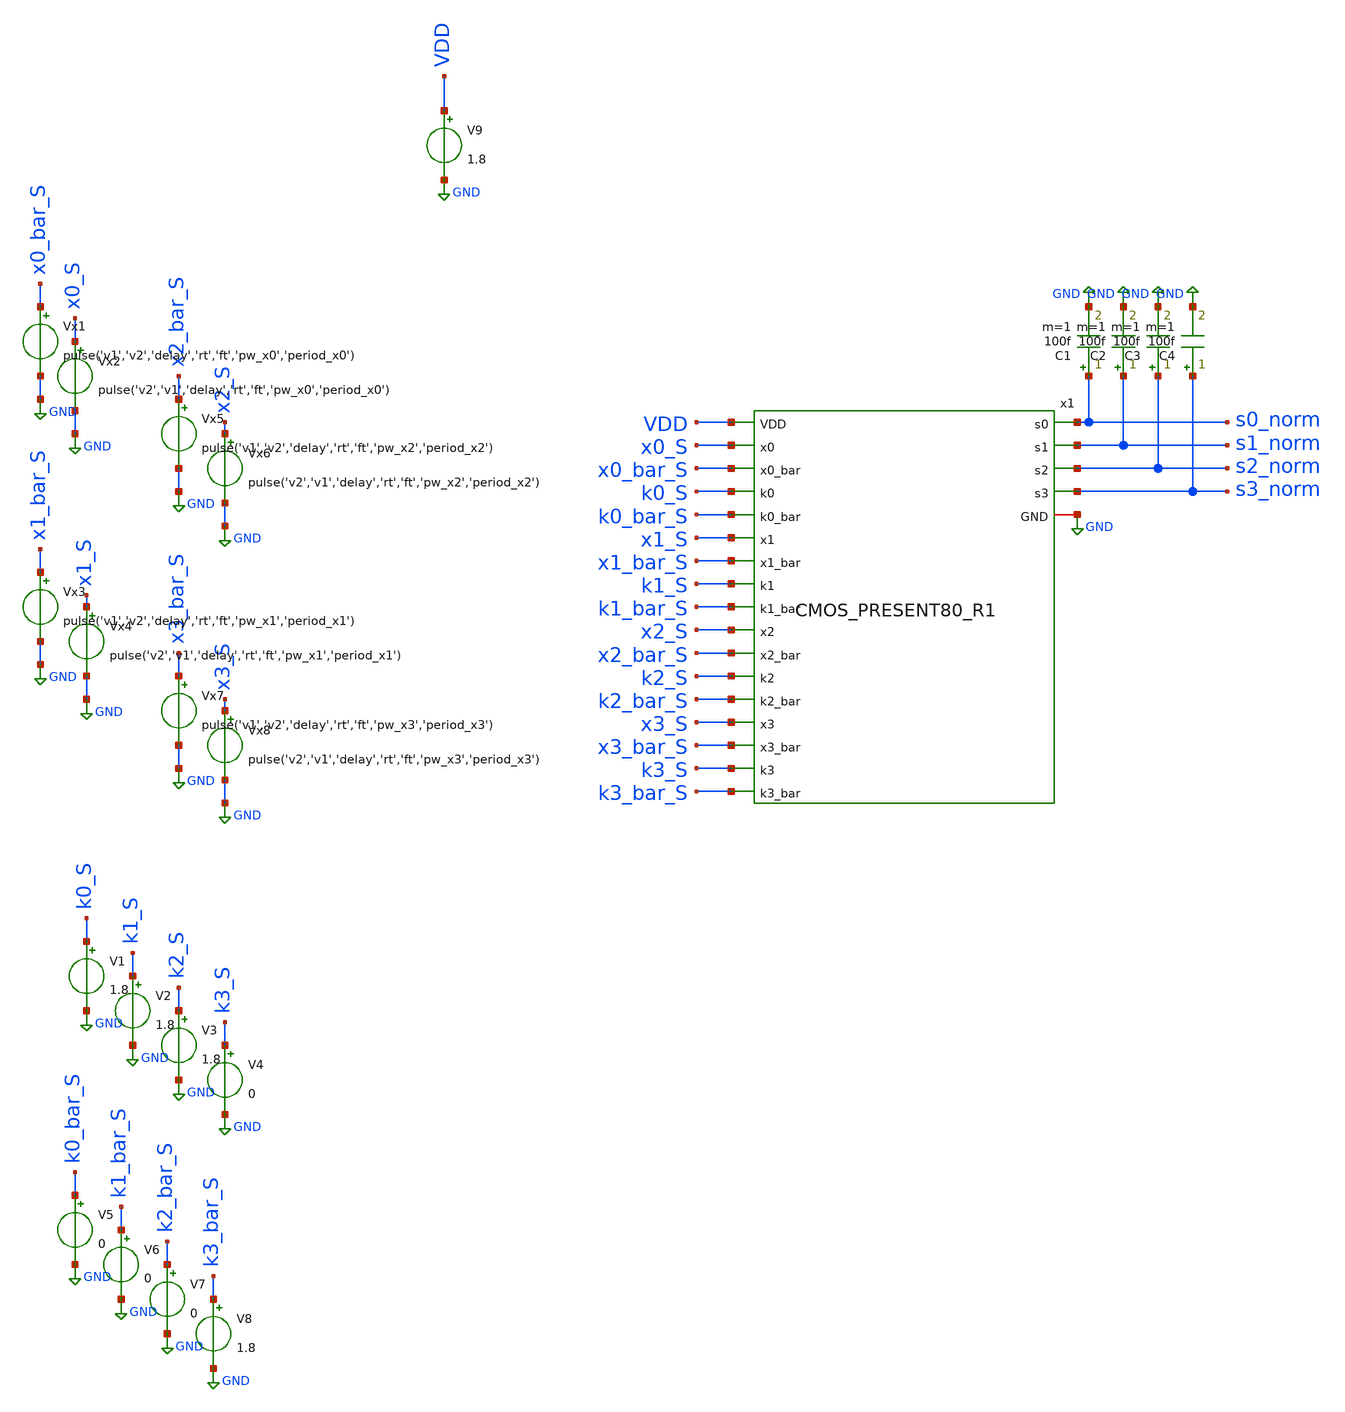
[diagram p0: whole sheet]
** sch_path: skywater_stuff/untitled-20.sch
**.subckt untitled-20
V9 VDD GND 1.8
C1 s0_norm GND 100f m=1
C2 s1_norm GND 100f m=1
C3 s2_norm GND 100f m=1
C4 s3_norm GND 100f m=1
x1 VDD GND k0_S k0_bar_S x0_S x0_bar_S x1_bar_S x1_S k1_bar_S k1_S k2_S k2_bar_S x2_S x2_bar_S
+ x3_bar_S x3_S k3_bar_S k3_S s3_norm s2_norm s1_norm s0_norm CMOS_PRESENT80_R1
V1 k0_S GND 1.8
V2 k1_S GND 1.8
V3 k2_S GND 1.8
V4 k3_S GND 0
V5 k0_bar_S GND 0
V6 k1_bar_S GND 0
V7 k2_bar_S GND 0
V8 k3_bar_S GND 1.8
Vx1 x0_bar_S GND pulse('v1','v2','delay','rt','ft','pw_x0','period_x0')
Vx2 x0_S GND pulse('v2','v1','delay','rt','ft','pw_x0','period_x0')
Vx3 x1_bar_S GND pulse('v1','v2','delay','rt','ft','pw_x1','period_x1')
Vx4 x1_S GND pulse('v2','v1','delay','rt','ft','pw_x1','period_x1')
Vx5 x2_bar_S GND pulse('v1','v2','delay','rt','ft','pw_x2','period_x2')
Vx6 x2_S GND pulse('v2','v1','delay','rt','ft','pw_x2','period_x2')
Vx7 x3_bar_S GND pulse('v1','v2','delay','rt','ft','pw_x3','period_x3')
Vx8 x3_S GND pulse('v2','v1','delay','rt','ft','pw_x3','period_x3')
**** begin user architecture code

.lib /research/pdk/open_pdks/share/pdk/sky130A/libs.tech/ngspice/sky130.lib.spice tt
**.include ~/magic_layout_stuff/CMOS_PRESENT80_R1.spice
**.include ~/magic_layout_stuff/CMOS_PRESENT80_R1_flat.spice
*.param v1='0' v2='1.8' delay='-1n' rt='50p' ft='50p' pw_x0='40n' period_x0='80n' pw_x1='80n' period_x1='160n'
*+ pw_x2='160n' period_x2='320n' pw_x3='320n' period_x3='640n'
.param v0 ='0' v0_bar ='1.8' v1 ='0' v1_bar ='1.8' v2 ='0' v2_bar ='1.8' v3 ='0' v3_bar ='1.8'
.option method=gear
.control
set tstart=0
set tstop=80n
let index=0
let index2=0
let start = $tstart
let stop = $tstop
let start_r2 = $tstop*200
let stop_r2 = ($tstop*200)+80n
*tran 0.1n 10u
*set v1_n = 0 v2_n = 1.8 delay_n = 0 rt_n = 50p ft_n = 50p
*set pw_x0n = 40n period_x0n = 80n pw_x1n = 80n period_x1n = 160n
*set pw_x2n = 160n period_x2n = 320n pw_x3n = 320n period_x3n = 640n

set value = 5
echo stuff

*alter Vx0 = 1.8
*plot v(s0_norm)
*snsave testfile.snap
let curr_time = index*80n
*stop when time =$&curr_time
*tran 1n 2u 0 1n
*alter Vx0 = 0
*delete 1
*let curr_time = 160n
*stop when time = $&curr_time
*echo $&curr_time
*echo start loop

while curr_time < 240n
	let index=index+1
	set  value = $&index
	*let trantime = time[0]
	*echo $&trantime
	echo going into altering
	foreach bit_index 0 1 2 3
		*echo $bit_index
		*echo `./test.sh $value $bit_index`
		set bit = `./test.sh $value $bit_index`
		alter Vx$bit_index = '$bit ? 1.8 : 0'
		alter Vx`echo $bit_index`_bar = '$bit ? 0 : 1.8'
		*alter @Vx4[pulse] = [ $v1 $v2 $delay   ]
		*alterparam v$bit_index = '$bit ? 1.8 : 0'
		*alterparam v`echo $bit_index`_bar = '$bit ? 0 : 1.8'
	end
	*alter Vx0=1.8
	echo test stuff
	let curr_time=index*80n
	*delete $&index
	stop when time=$&curr_time
	echo $&curr_time
	*break
	plot v(x0_s)
	if curr_time = 80ns
		tran 1n 2u 0 1n
	else
		resume
	end

end

*let Pinst = v(VDD)*v9#branch
*wrdata K7_32u_50cycle.csv Pinst
*while index < 401
*	let Pinst = v(VDD)*v9#branch
	*plot Pinst
*	let lin-tstart = start
*	let lin-tstop = stop
*	let lin-tstep = 0.01n
*	linearize Pinst
	*plot v(pinst)
	*display
*	set appendwrite
	wrdata samp_interval_K0_32u_50cycle_minus1ns.csv Pinst
	*wrdata samp_interval_K1_32u_50cycle_minus1ns.csv Pinst
	*wrdata samp_interval_K2_32u_50cycle_minus1ns.csv Pinst
	*wrdata samp_interval_K3_32u_50cycle_minus1ns.csv Pinst
	*wrdata samp_interval_K4_32u_50cycle_minus1ns.csv Pinst
	*wrdata samp_interval_K5_32u_50cycle_minus1ns.csv Pinst
	*wrdata samp_interval_K6_32u_50cycle_minus1ns.csv Pinst
	*wrdata samp_interval_K7_32u_50cycle_minus1ns.csv Pinst
	*wrdata samp_interval_K8_32u_50cycle_minus1ns.csv Pinst
	*wrdata samp_interval_K9_32u_50cycle_minus1ns.csv Pinst
	*wrdata samp_interval_K10_32u_50cycle_minus1ns.csv Pinst
	*wrdata samp_interval_K11_32u_50cycle_minus1ns.csv Pinst
	*wrdata samp_interval_K12_32u_50cycle_minus1ns.csv Pinst
	*wrdata samp_interval_K13_32u_50cycle_minus1ns.csv Pinst
	*wrdata samp_interval_K14_32u_50cycle_minus1ns.csv Pinst
	*wrdata samp_interval_K15_32u_50cycle_minus1ns.csv Pinst
*	*wrdata samp_interval_6p4u_10cycle.csv Pinst
*	let start = stop
*	let stop = stop+80n
*	let index = index + 1
*	*echo $plots
*	setplot tran1
*	destroy tran2
*	*echo $plots
*end

*while index2 < 201
*	tran 0.7u 34u 0 1u
*	let Pinst = v(VDD)*v9#branch
*	let lin-tstart = start_r2
*	let lin-tstop = stop_r2
*	let lin-tstep = 1n
*	linearize Pinst
*	*plot Pinst
*	set appendwrite
*	wrdata samp_interval_32u_50cycle.csv Pinst
*	*wrdata samp_interval_6p4u_10cycle.csv Pinst
*	let start_r2 = stop_r2
*	let stop_r2 = stop_r2+80n
*	let index2 = index2 + 1
*end
.endc


**** end user architecture code
**.ends
.GLOBAL GND
.end
